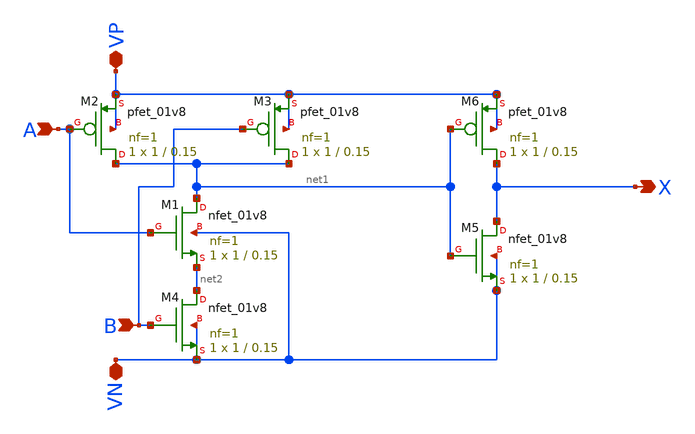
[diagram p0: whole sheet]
** sch_path: projekat_spice/layout/and/AND.sch
**.subckt AND A B VN VP X
*.ipin A
*.ipin B
*.iopin VN
*.iopin VP
*.opin X
XM1 net1 A net2 VN sky130_fd_pr__nfet_01v8 L=0.15 W=1 nf=1 ad='int((nf+1)/2) * W/nf * 0.29' as='int((nf+2)/2) * W/nf * 0.29'
+ pd='2*int((nf+1)/2) * (W/nf + 0.29)' ps='2*int((nf+2)/2) * (W/nf + 0.29)' nrd='0.29 / W' nrs='0.29 / W'
+ sa=0 sb=0 sd=0 mult=1 m=1
XM2 net1 A VP VP sky130_fd_pr__pfet_01v8 L=0.15 W=1 nf=1 ad='int((nf+1)/2) * W/nf * 0.29' as='int((nf+2)/2) * W/nf * 0.29'
+ pd='2*int((nf+1)/2) * (W/nf + 0.29)' ps='2*int((nf+2)/2) * (W/nf + 0.29)' nrd='0.29 / W' nrs='0.29 / W'
+ sa=0 sb=0 sd=0 mult=1 m=1
XM3 net1 B VP VP sky130_fd_pr__pfet_01v8 L=0.15 W=1 nf=1 ad='int((nf+1)/2) * W/nf * 0.29' as='int((nf+2)/2) * W/nf * 0.29'
+ pd='2*int((nf+1)/2) * (W/nf + 0.29)' ps='2*int((nf+2)/2) * (W/nf + 0.29)' nrd='0.29 / W' nrs='0.29 / W'
+ sa=0 sb=0 sd=0 mult=1 m=1
XM4 net2 B VN VN sky130_fd_pr__nfet_01v8 L=0.15 W=1 nf=1 ad='int((nf+1)/2) * W/nf * 0.29' as='int((nf+2)/2) * W/nf * 0.29'
+ pd='2*int((nf+1)/2) * (W/nf + 0.29)' ps='2*int((nf+2)/2) * (W/nf + 0.29)' nrd='0.29 / W' nrs='0.29 / W'
+ sa=0 sb=0 sd=0 mult=1 m=1
XM5 X net1 VN VN sky130_fd_pr__nfet_01v8 L=0.15 W=1 nf=1 ad='int((nf+1)/2) * W/nf * 0.29' as='int((nf+2)/2) * W/nf * 0.29'
+ pd='2*int((nf+1)/2) * (W/nf + 0.29)' ps='2*int((nf+2)/2) * (W/nf + 0.29)' nrd='0.29 / W' nrs='0.29 / W'
+ sa=0 sb=0 sd=0 mult=1 m=1
XM6 X net1 VP VP sky130_fd_pr__pfet_01v8 L=0.15 W=1 nf=1 ad='int((nf+1)/2) * W/nf * 0.29' as='int((nf+2)/2) * W/nf * 0.29'
+ pd='2*int((nf+1)/2) * (W/nf + 0.29)' ps='2*int((nf+2)/2) * (W/nf + 0.29)' nrd='0.29 / W' nrs='0.29 / W'
+ sa=0 sb=0 sd=0 mult=1 m=1
**.ends
.end
